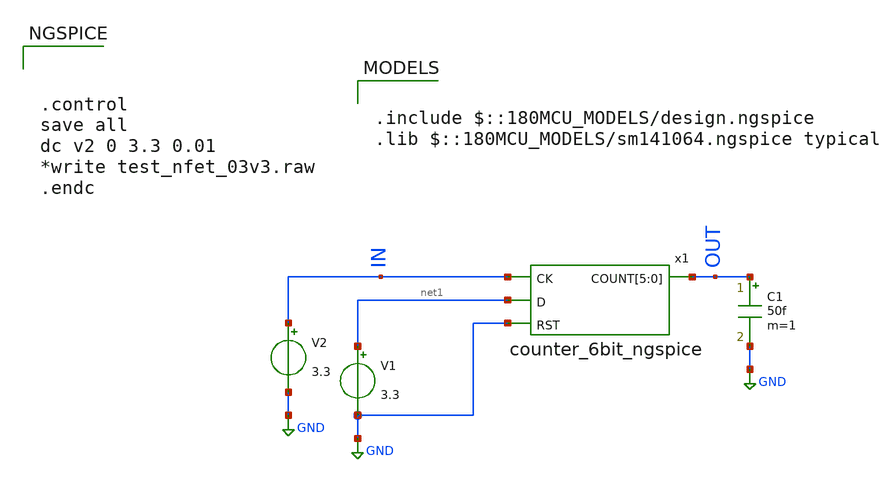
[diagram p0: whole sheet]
** sch_path: Clock_Generator_PAKISTAN_02/Schematics/counter_TB.sch
* StefanSchippers/xschem/xschem_library/ngspice/and_ngspice.sch:
* Copyright (C) 1998-2023 Stefan Frederik Schippers
* This program is free software; you can redistribute it and/or modify
* it under the terms of the GNU General Public License as published by
* the Free Software Foundation; either version 2 of the License, or
* (at your option) any later version.
**.subckt counter_TB
x1 IN OUT OUT OUT OUT OUT OUT net1 GND counter_6bit_ngspice
C1 OUT GND 50f m=1
V2 IN GND 3.3
V1 net1 GND 3.3
**** begin user architecture code



.control
save all
dc v2 0 3.3 0.01
*write test_nfet_03v3.raw
.endc



.include $::180MCU_MODELS/design.ngspice
.lib $::180MCU_MODELS/sm141064.ngspice typical

**** end user architecture code
**.ends

* expanding   symbol:  /home/shahid/EDA_TOOLs/xschem/xschem_library/ngspice/counter_6bit_ngspice.sym
*+ # of pins=4
** sym_path: /home/shahid/EDA_TOOLs/xschem/xschem_library/ngspice/counter_6bit_ngspice.sym
** sch_path: /home/shahid/EDA_TOOLs/xschem/xschem_library/ngspice/counter_6bit_ngspice.sch
.subckt counter_6bit_ngspice CK COUNT[5] COUNT[4] COUNT[3] COUNT[2] COUNT[1] COUNT[0] D RST
*.ipin RST
*.ipin D
*.opin COUNT[5],COUNT[4],COUNT[3],COUNT[2],COUNT[1],COUNT[0]
*.ipin CK
x2[5] S[5] CK COUNT[5] RST flip_flop_ngspice
x2[4] S[4] CK COUNT[4] RST flip_flop_ngspice
x2[3] S[3] CK COUNT[3] RST flip_flop_ngspice
x2[2] S[2] CK COUNT[2] RST flip_flop_ngspice
x2[1] S[1] CK COUNT[1] RST flip_flop_ngspice
x2[0] S[0] CK COUNT[0] RST flip_flop_ngspice
x1[5] COUNT[5] S[5] COUT[5] COUT[4] half_adder_ngspice
x1[4] COUNT[4] S[4] COUT[4] COUT[3] half_adder_ngspice
x1[3] COUNT[3] S[3] COUT[3] COUT[2] half_adder_ngspice
x1[2] COUNT[2] S[2] COUT[2] COUT[1] half_adder_ngspice
x1[1] COUNT[1] S[1] COUT[1] COUT[0] half_adder_ngspice
x1[0] COUNT[0] S[0] COUT[0] D half_adder_ngspice
.ends


* expanding   symbol:  flip_flop_ngspice.sym # of pins=4
** sym_path: flip_flop_ngspice.sym
** sch_path: flip_flop_ngspice.sch
.subckt flip_flop_ngspice D CLK Q RST
*.ipin D
*.ipin CLK
*.ipin RST
*.opin Q
x2 DI keeper_ngspice
S1 net2 net3 VCC CLK SWITCH
S2 QI net1 CLK 0 SWITCH
x3 QI keeper_ngspice
x4 Q QI buf_ngspice ROUT=100
S3 QI 0 RST 0 SWITCH
x1 net1 DI buf_ngspice ROUT=1000
S4 DI net2 VCC RST SWITCH
S5 DI 0 RST 0 SWITCH
x5 net3 D buf_ngspice ROUT=1000
.ends


* expanding   symbol:  half_adder_ngspice.sym # of pins=4
** sym_path: half_adder_ngspice.sym
** sch_path: half_adder_ngspice.sch
.subckt half_adder_ngspice A S COUT B
*.ipin A
*.ipin B
*.opin S
*.opin COUT
x1 S A B xor_ngspice ROUT=1000
x2 COUT A B and_ngspice ROUT=1000
.ends


* expanding   symbol:  keeper_ngspice.sym # of pins=1
** sym_path: keeper_ngspice.sym
** sch_path: keeper_ngspice.sch
.subckt keeper_ngspice A
*.ipin A
x1 Y A inv_ngspice ROUT=1000
x2 A Y inv_ngspice ROUT=300k
.ends


* expanding   symbol:  buf_ngspice.sym # of pins=2
** sym_path: buf_ngspice.sym
** sch_path: buf_ngspice.sch
.subckt buf_ngspice Y A  ROUT=1000
*.ipin A
*.opin Y
B1 net1 0 V = 'VCC/2*(1+tanh((V(A1)-VCC/2)*100))'
R1 Y1 net1 ROUT m=1
C3 Y1 0 8f m=1
C1 A1 0 4f m=1
V1 Y Y1 0
V2 A1 A 0
.ends


* expanding   symbol:  xor_ngspice.sym # of pins=3
** sym_path: xor_ngspice.sym
** sch_path: xor_ngspice.sch
.subckt xor_ngspice Y A B  ROUT=1000
*.ipin A
*.opin Y
*.ipin B
B1 net1 0 V = 'VCC/2*(1+tanh((abs(V(A1)-V(B1))-VCC/2)*100))'
R1 Y1 net1 'ROUT' m=1
C1 A1 0 8f m=1
C2 B1 0 8f m=1
C3 Y1 0 8f m=1
V1 A1 A 0
V2 B1 B 0
V3 Y Y1 0
.ends


* expanding   symbol:  and_ngspice.sym # of pins=3
** sym_path: and_ngspice.sym
** sch_path: and_ngspice.sch
.subckt and_ngspice Y A B  ROUT=1000
*.ipin A
*.opin Y
*.ipin B
B1 net1 0 V = 'VCC/2*(1+tanh((min(V(A1),V(B1))-VCC/2)*100))'
R1 Y1 net1 'ROUT' m=1
C1 A1 0 8f m=1
C2 B1 0 8f m=1
C3 Y1 0 8f m=1
V1 A1 A 0
V2 B1 B 0
V3 Y Y1 0
.ends


* expanding   symbol:  inv_ngspice.sym # of pins=2
** sym_path: inv_ngspice.sym
** sch_path: inv_ngspice.sch
.subckt inv_ngspice Y A  ROUT=1000
*.ipin A
*.opin Y
B1 net1 0 V = 'VCC/2*(1-tanh((V(A1)-VCC/2)*100))'
R1 Y1 net1 'ROUT' m=1
C1 A1 0 8f m=1
C2 Y1 0 8f m=1
V1 Y Y1 0
V2 A1 A 0
.ends

.GLOBAL GND
.end
